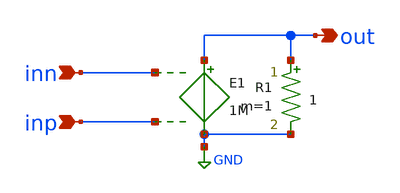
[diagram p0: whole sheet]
** sch_path: 2_ideal_circuits/ideal_opamp.sch
**.subckt ideal_opamp inn inp out
*.ipin inn
*.ipin inp
*.opin out
E1 out GND inn inp 1M
R1 out GND 1 m=1
**.ends
.GLOBAL GND
.end
